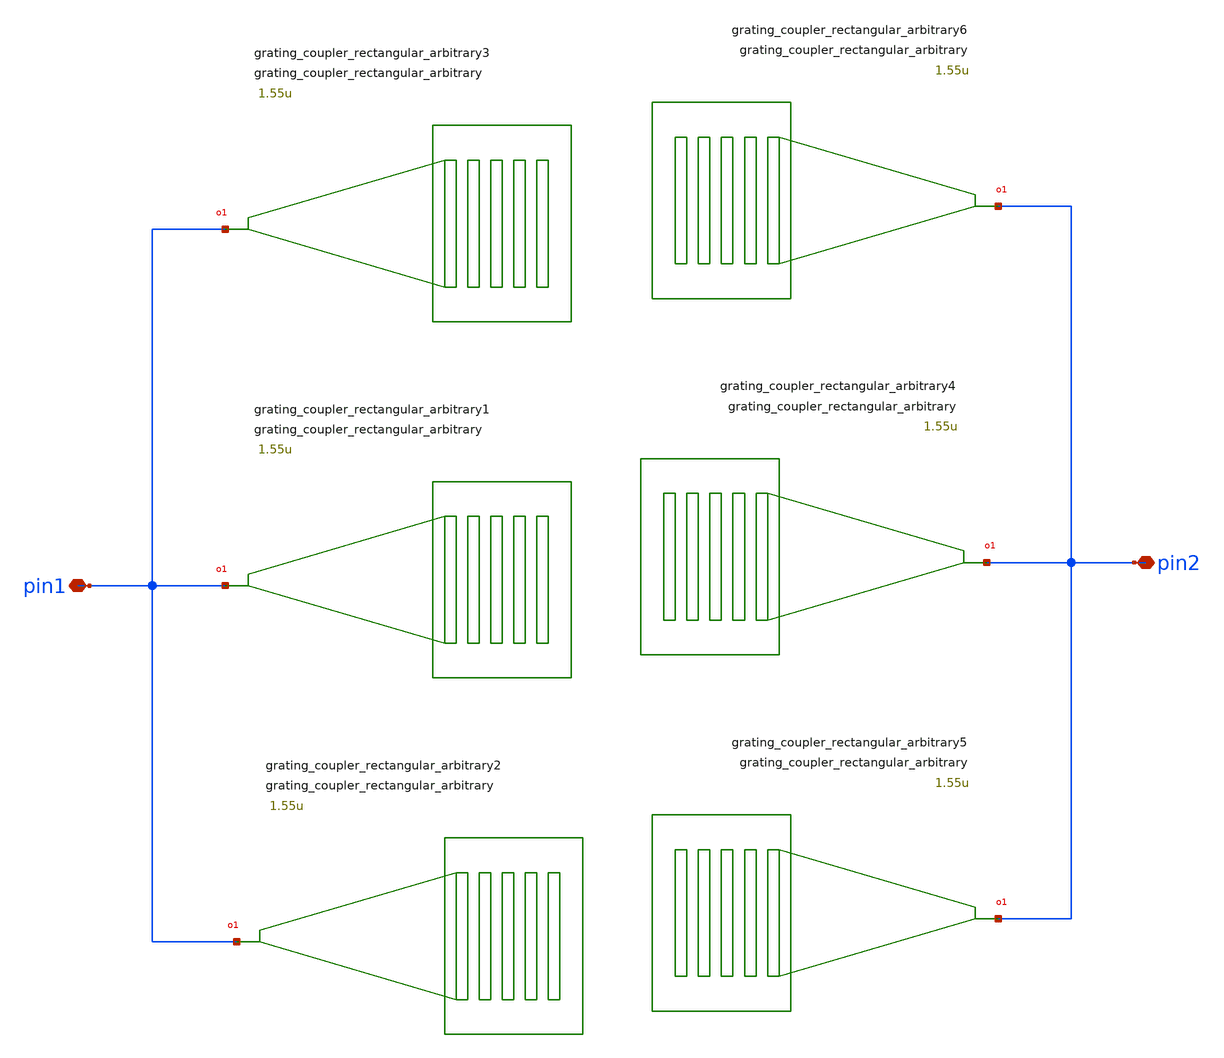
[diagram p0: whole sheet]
** sch_path: xschem/tests/test_sch/test_grating_coupler_rectangular_arbitrary.sch
* Copyright (c) 2024, Mabrains LLC
* Licensed under the GNU Lesser General Public License, Version 3.0 (the "License");
* you may not use this file except in compliance with the License.
* GNU Lesser General Public License
* Version 3, 29 June 2007
* This program is free software: you can redistribute it and/or modify
* it under the terms of the GNU Lesser General Public License as published
* by the Free Software Foundation, either version 3 of the License, or
* (at your option) any later version.
* This program is distributed in the hope that it will be useful,
* but WITHOUT ANY WARRANTY; without even the implied warranty of
* MERCHANTABILITY or FITNESS FOR A PARTICULAR PURPOSE.  See the
* GNU Lesser General Public License for more details.
* You should have received a copy of the GNU Lesser General Public License
* along with this program.  If not, see <https://www.gnu.org/licenses/>.
* SPDX-License-Identifier: LGPL-3.0
**.subckt test_grating_coupler_rectangular_arbitrary pin1 pin2
*.iopin pin1
*.iopin pin2
Pgrating_coupler_rectangular_arbitrary1 pin1 grating_coupler_rectangular_arbitrary gaps=[0.2u, 0.2u,
+ 0.2u, 0.2u, 0.2u, 0.2u, 0.2u, 0.2u, 0.2u, 0.2u] widths=[0.5u, 0.5u, 0.5u, 0.5u, 0.5u, 0.5u, 0.5u, 0.5u,
+ 0.5u, 0.5u] width_grating=11.0u length_taper=150.0u wavelength=1.55u slab_xmin=-1.0u slab_offset=1.0u
+ fiber_angle=15
Pgrating_coupler_rectangular_arbitrary2 pin1 grating_coupler_rectangular_arbitrary gaps=[0.2u, 0.2u,
+ 0.2u, 0.2u, 0.2u, 0.2u, 0.2u, 0.2u, 0.2u, 0.2u] widths=[0.5u, 0.5u, 0.5u, 0.5u, 0.5u, 0.5u, 0.5u, 0.5u,
+ 0.5u, 0.5u] width_grating=11.0u length_taper=150.0u wavelength=1.55u slab_xmin=-1.0u slab_offset=1.0u
+ fiber_angle=15
Pgrating_coupler_rectangular_arbitrary3 pin1 grating_coupler_rectangular_arbitrary gaps=[0.2u, 0.2u,
+ 0.2u, 0.2u, 0.2u, 0.2u, 0.2u, 0.2u, 0.2u, 0.2u] widths=[0.5u, 0.5u, 0.5u, 0.5u, 0.5u, 0.5u, 0.5u, 0.5u,
+ 0.5u, 0.5u] width_grating=11.0u length_taper=150.0u wavelength=1.55u slab_xmin=-1.0u slab_offset=1.0u
+ fiber_angle=15
Pgrating_coupler_rectangular_arbitrary4 pin2 grating_coupler_rectangular_arbitrary gaps=[0.2u, 0.2u,
+ 0.2u, 0.2u, 0.2u, 0.2u, 0.2u, 0.2u, 0.2u, 0.2u] widths=[0.5u, 0.5u, 0.5u, 0.5u, 0.5u, 0.5u, 0.5u, 0.5u,
+ 0.5u, 0.5u] width_grating=11.0u length_taper=150.0u wavelength=1.55u slab_xmin=-1.0u slab_offset=1.0u
+ fiber_angle=15
Pgrating_coupler_rectangular_arbitrary5 pin2 grating_coupler_rectangular_arbitrary gaps=[0.2u, 0.2u,
+ 0.2u, 0.2u, 0.2u, 0.2u, 0.2u, 0.2u, 0.2u, 0.2u] widths=[0.5u, 0.5u, 0.5u, 0.5u, 0.5u, 0.5u, 0.5u, 0.5u,
+ 0.5u, 0.5u] width_grating=11.0u length_taper=150.0u wavelength=1.55u slab_xmin=-1.0u slab_offset=1.0u
+ fiber_angle=15
Pgrating_coupler_rectangular_arbitrary6 pin2 grating_coupler_rectangular_arbitrary gaps=[0.2u, 0.2u,
+ 0.2u, 0.2u, 0.2u, 0.2u, 0.2u, 0.2u, 0.2u, 0.2u] widths=[0.5u, 0.5u, 0.5u, 0.5u, 0.5u, 0.5u, 0.5u, 0.5u,
+ 0.5u, 0.5u] width_grating=11.0u length_taper=150.0u wavelength=1.55u slab_xmin=-1.0u slab_offset=1.0u
+ fiber_angle=15
**.ends
.end
